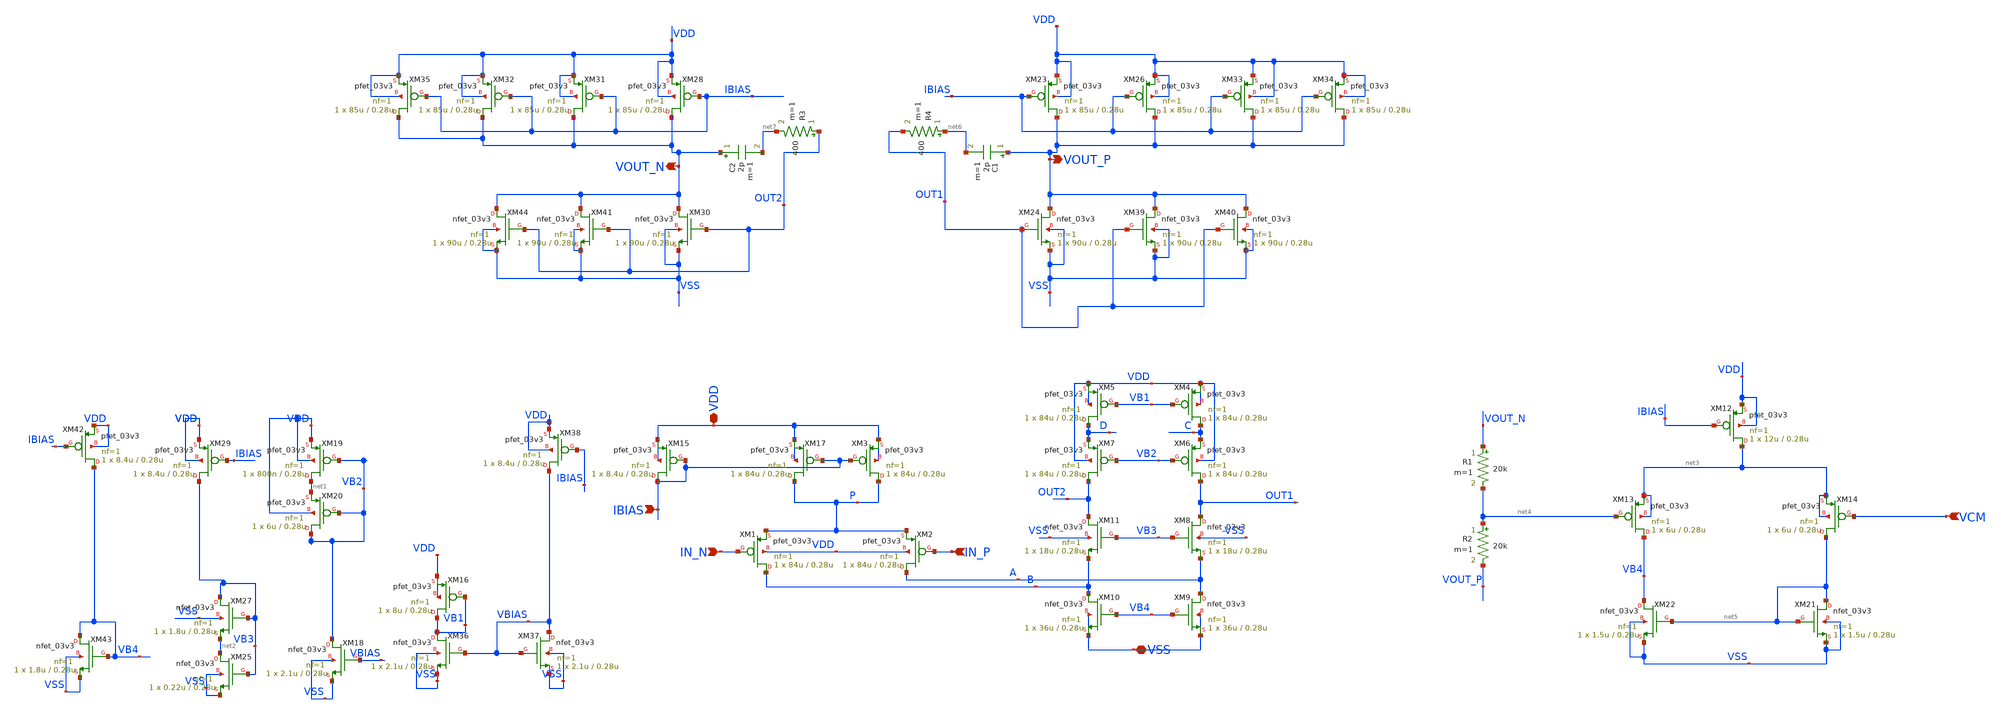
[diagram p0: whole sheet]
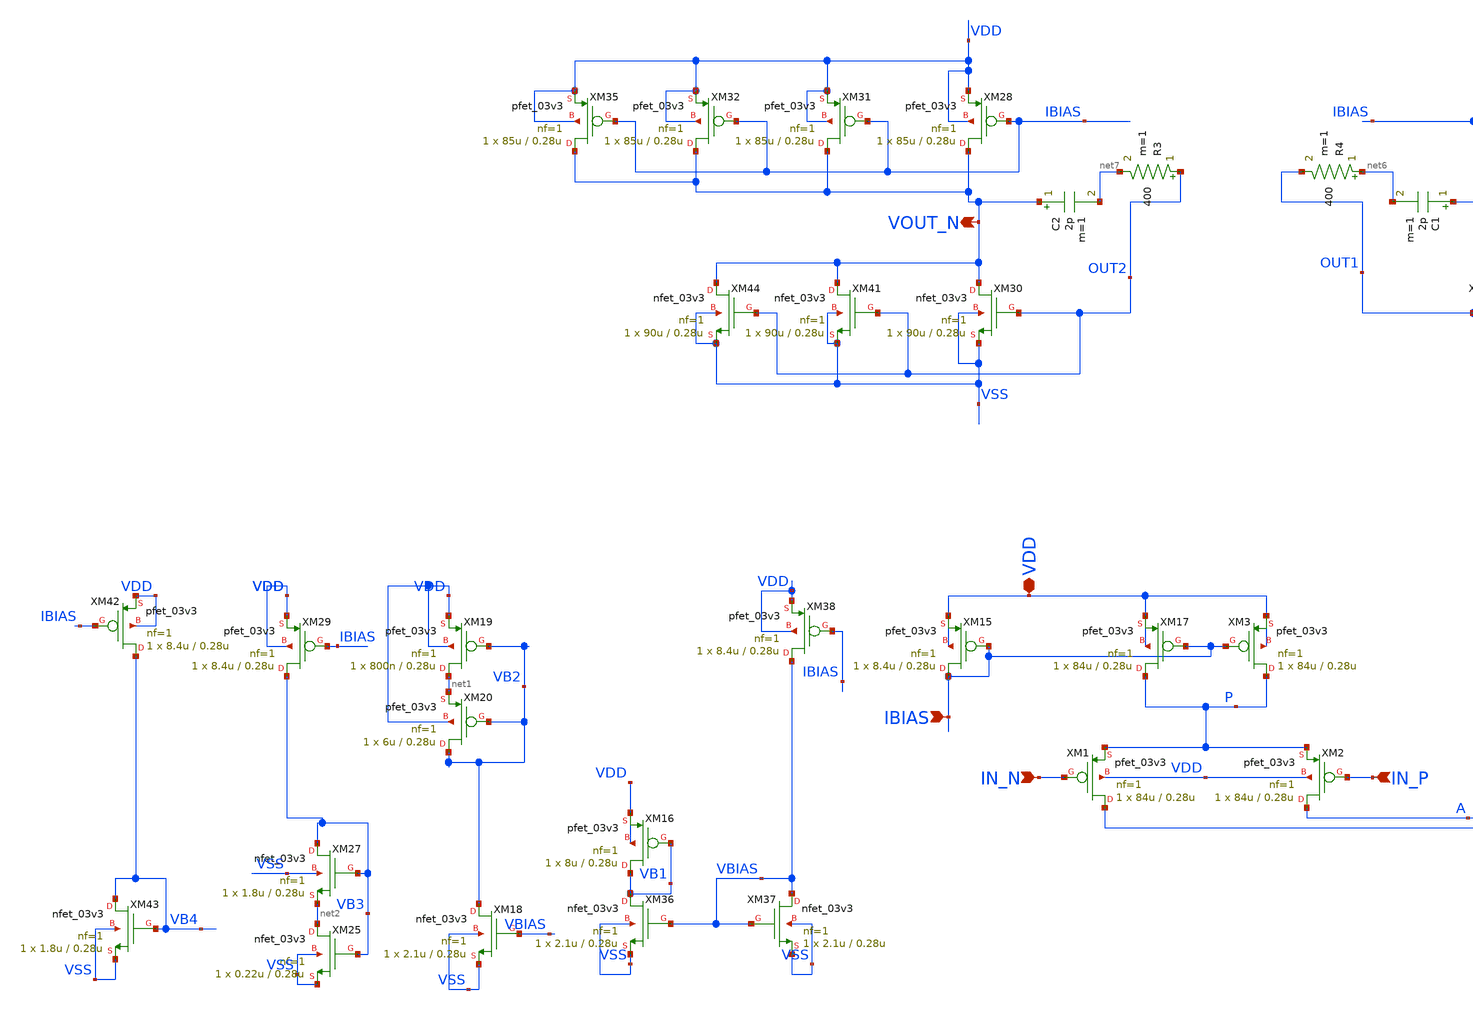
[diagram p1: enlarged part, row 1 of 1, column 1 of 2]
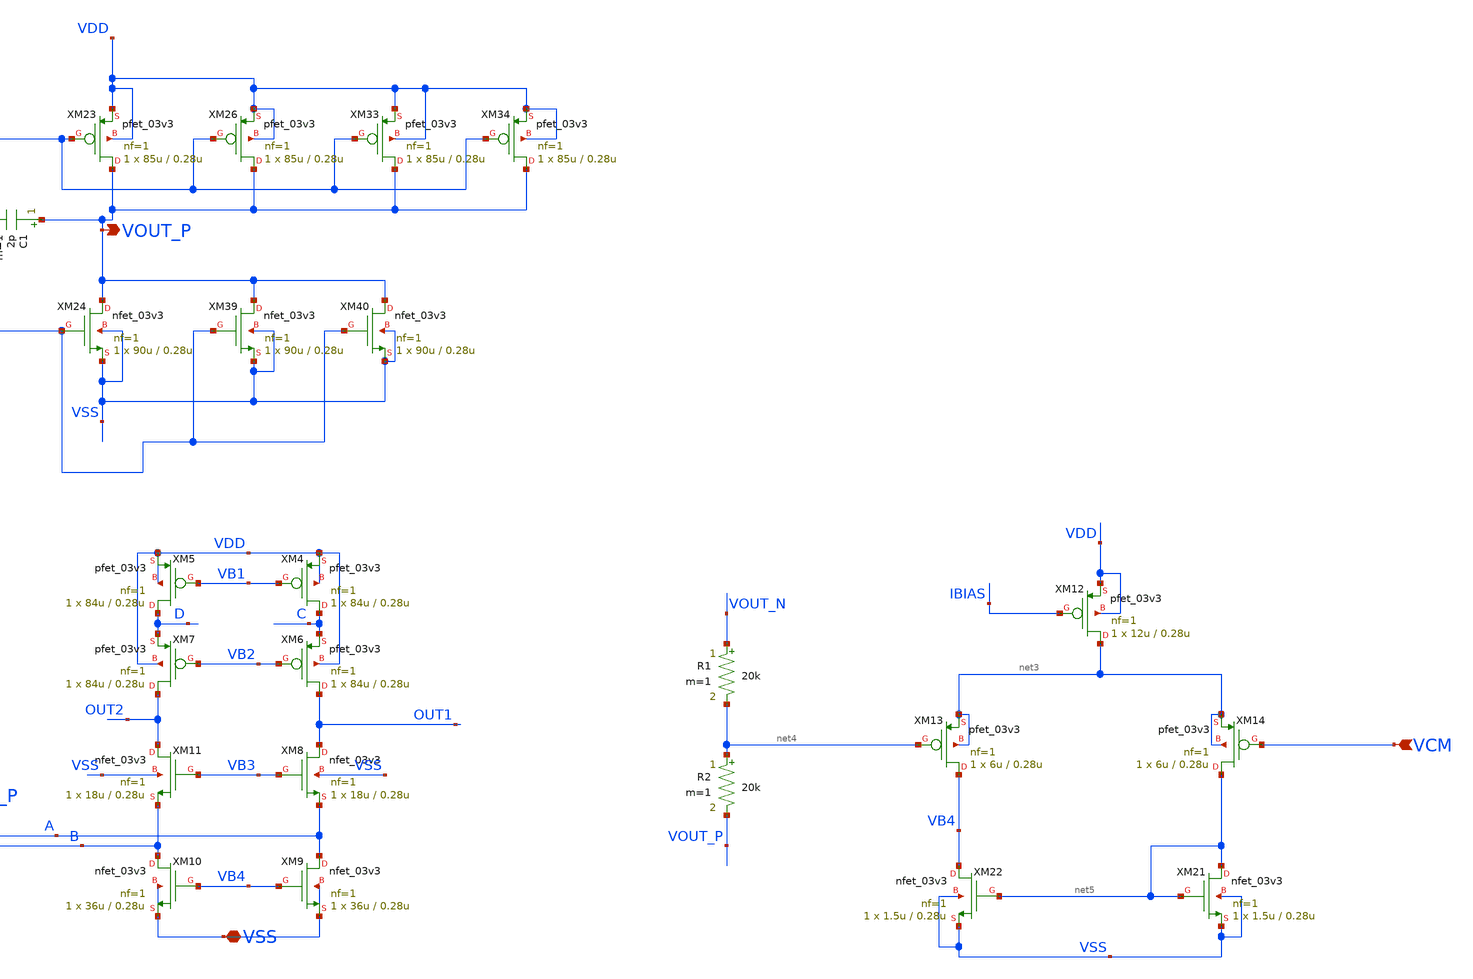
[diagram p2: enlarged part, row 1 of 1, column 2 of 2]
** sch_path: AWG_OUTPUT_AND_MUX_PAKISTAN_05/xschem/OPAMP_PMOS_FINAL1.sch
**.subckt OPAMP_PMOS_FINAL1 VDD VOUT_P VOUT_N VSS IN_N IN_P IBIAS VCM
*.iopin VDD
*.opin VOUT_P
*.opin VOUT_N
*.iopin VSS
*.ipin IN_N
*.ipin IN_P
*.ipin IBIAS
*.ipin VCM
XM1 B IN_N P VDD pfet_03v3 L=0.28u W=84u nf=1 ad='int((nf+1)/2) * W/nf * 0.18u' as='int((nf+2)/2) * W/nf * 0.18u'
+ pd='2*int((nf+1)/2) * (W/nf + 0.18u)' ps='2*int((nf+2)/2) * (W/nf + 0.18u)' nrd='0.18u / W' nrs='0.18u / W'
+ sa=0 sb=0 sd=0 m=1
XM2 A IN_P P VDD pfet_03v3 L=0.28u W=84u nf=1 ad='int((nf+1)/2) * W/nf * 0.18u' as='int((nf+2)/2) * W/nf * 0.18u'
+ pd='2*int((nf+1)/2) * (W/nf + 0.18u)' ps='2*int((nf+2)/2) * (W/nf + 0.18u)' nrd='0.18u / W' nrs='0.18u / W'
+ sa=0 sb=0 sd=0 m=1
XM3 P IBIAS VDD VDD pfet_03v3 L=0.28u W=84u nf=1 ad='int((nf+1)/2) * W/nf * 0.18u' as='int((nf+2)/2) * W/nf * 0.18u'
+ pd='2*int((nf+1)/2) * (W/nf + 0.18u)' ps='2*int((nf+2)/2) * (W/nf + 0.18u)' nrd='0.18u / W' nrs='0.18u / W'
+ sa=0 sb=0 sd=0 m=1
XM4 C VB1 VDD VDD pfet_03v3 L=0.28u W=84u nf=1 ad='int((nf+1)/2) * W/nf * 0.18u' as='int((nf+2)/2) * W/nf * 0.18u'
+ pd='2*int((nf+1)/2) * (W/nf + 0.18u)' ps='2*int((nf+2)/2) * (W/nf + 0.18u)' nrd='0.18u / W' nrs='0.18u / W'
+ sa=0 sb=0 sd=0 m=1
XM5 D VB1 VDD VDD pfet_03v3 L=0.28u W=84u nf=1 ad='int((nf+1)/2) * W/nf * 0.18u' as='int((nf+2)/2) * W/nf * 0.18u'
+ pd='2*int((nf+1)/2) * (W/nf + 0.18u)' ps='2*int((nf+2)/2) * (W/nf + 0.18u)' nrd='0.18u / W' nrs='0.18u / W'
+ sa=0 sb=0 sd=0 m=1
XM6 OUT1 VB2 C VDD pfet_03v3 L=0.28u W=84u nf=1 ad='int((nf+1)/2) * W/nf * 0.18u' as='int((nf+2)/2) * W/nf * 0.18u'
+ pd='2*int((nf+1)/2) * (W/nf + 0.18u)' ps='2*int((nf+2)/2) * (W/nf + 0.18u)' nrd='0.18u / W' nrs='0.18u / W'
+ sa=0 sb=0 sd=0 m=1
XM7 OUT2 VB2 D VDD pfet_03v3 L=0.28u W=84u nf=1 ad='int((nf+1)/2) * W/nf * 0.18u' as='int((nf+2)/2) * W/nf * 0.18u'
+ pd='2*int((nf+1)/2) * (W/nf + 0.18u)' ps='2*int((nf+2)/2) * (W/nf + 0.18u)' nrd='0.18u / W' nrs='0.18u / W'
+ sa=0 sb=0 sd=0 m=1
XM8 OUT1 VB3 A VSS nfet_03v3 L=0.28u W=18u nf=1 ad='int((nf+1)/2) * W/nf * 0.18u' as='int((nf+2)/2) * W/nf * 0.18u'
+ pd='2*int((nf+1)/2) * (W/nf + 0.18u)' ps='2*int((nf+2)/2) * (W/nf + 0.18u)' nrd='0.18u / W' nrs='0.18u / W'
+ sa=0 sb=0 sd=0 m=1
XM9 A VB4 VSS VSS nfet_03v3 L=0.28u W=36u nf=1 ad='int((nf+1)/2) * W/nf * 0.18u' as='int((nf+2)/2) * W/nf * 0.18u'
+ pd='2*int((nf+1)/2) * (W/nf + 0.18u)' ps='2*int((nf+2)/2) * (W/nf + 0.18u)' nrd='0.18u / W' nrs='0.18u / W'
+ sa=0 sb=0 sd=0 m=1
XM10 B VB4 VSS VSS nfet_03v3 L=0.28u W=36u nf=1 ad='int((nf+1)/2) * W/nf * 0.18u' as='int((nf+2)/2) * W/nf * 0.18u'
+ pd='2*int((nf+1)/2) * (W/nf + 0.18u)' ps='2*int((nf+2)/2) * (W/nf + 0.18u)' nrd='0.18u / W' nrs='0.18u / W'
+ sa=0 sb=0 sd=0 m=1
XM17 P IBIAS VDD VDD pfet_03v3 L=0.28u W=84u nf=1 ad='int((nf+1)/2) * W/nf * 0.18u' as='int((nf+2)/2) * W/nf * 0.18u'
+ pd='2*int((nf+1)/2) * (W/nf + 0.18u)' ps='2*int((nf+2)/2) * (W/nf + 0.18u)' nrd='0.18u / W' nrs='0.18u / W'
+ sa=0 sb=0 sd=0 m=1
XM11 OUT2 VB3 B VSS nfet_03v3 L=0.28u W=18u nf=1 ad='int((nf+1)/2) * W/nf * 0.18u' as='int((nf+2)/2) * W/nf * 0.18u'
+ pd='2*int((nf+1)/2) * (W/nf + 0.18u)' ps='2*int((nf+2)/2) * (W/nf + 0.18u)' nrd='0.18u / W' nrs='0.18u / W'
+ sa=0 sb=0 sd=0 m=1
XM36 VB1 VBIAS VSS VSS nfet_03v3 L=0.28u W=2.1u nf=1 ad='int((nf+1)/2) * W/nf * 0.18u' as='int((nf+2)/2) * W/nf * 0.18u'
+ pd='2*int((nf+1)/2) * (W/nf + 0.18u)' ps='2*int((nf+2)/2) * (W/nf + 0.18u)' nrd='0.18u / W' nrs='0.18u / W'
+ sa=0 sb=0 sd=0 m=1
XM37 VBIAS VBIAS VSS VSS nfet_03v3 L=0.28u W=2.1u nf=1 ad='int((nf+1)/2) * W/nf * 0.18u' as='int((nf+2)/2) * W/nf * 0.18u'
+ pd='2*int((nf+1)/2) * (W/nf + 0.18u)' ps='2*int((nf+2)/2) * (W/nf + 0.18u)' nrd='0.18u / W' nrs='0.18u / W'
+ sa=0 sb=0 sd=0 m=1
XM38 VBIAS IBIAS VDD VDD pfet_03v3 L=0.28u W=8.4u nf=1 ad='int((nf+1)/2) * W/nf * 0.18u' as='int((nf+2)/2) * W/nf * 0.18u'
+ pd='2*int((nf+1)/2) * (W/nf + 0.18u)' ps='2*int((nf+2)/2) * (W/nf + 0.18u)' nrd='0.18u / W' nrs='0.18u / W'
+ sa=0 sb=0 sd=0 m=1
XM42 VB4 IBIAS VDD VDD pfet_03v3 L=0.28u W=8.4u nf=1 ad='int((nf+1)/2) * W/nf * 0.18u' as='int((nf+2)/2) * W/nf * 0.18u'
+ pd='2*int((nf+1)/2) * (W/nf + 0.18u)' ps='2*int((nf+2)/2) * (W/nf + 0.18u)' nrd='0.18u / W' nrs='0.18u / W'
+ sa=0 sb=0 sd=0 m=1
XM43 VB4 VB4 VSS VSS nfet_03v3 L=0.28u W=1.8u nf=1 ad='int((nf+1)/2) * W/nf * 0.18u' as='int((nf+2)/2) * W/nf * 0.18u'
+ pd='2*int((nf+1)/2) * (W/nf + 0.18u)' ps='2*int((nf+2)/2) * (W/nf + 0.18u)' nrd='0.18u / W' nrs='0.18u / W'
+ sa=0 sb=0 sd=0 m=1
XM15 IBIAS IBIAS VDD VDD pfet_03v3 L=0.28u W=8.4u nf=1 ad='int((nf+1)/2) * W/nf * 0.18u' as='int((nf+2)/2) * W/nf * 0.18u'
+ pd='2*int((nf+1)/2) * (W/nf + 0.18u)' ps='2*int((nf+2)/2) * (W/nf + 0.18u)' nrd='0.18u / W' nrs='0.18u / W'
+ sa=0 sb=0 sd=0 m=1
XM16 VB1 VB1 VDD VDD pfet_03v3 L=0.28u W=8u nf=1 ad='int((nf+1)/2) * W/nf * 0.18u' as='int((nf+2)/2) * W/nf * 0.18u'
+ pd='2*int((nf+1)/2) * (W/nf + 0.18u)' ps='2*int((nf+2)/2) * (W/nf + 0.18u)' nrd='0.18u / W' nrs='0.18u / W'
+ sa=0 sb=0 sd=0 m=1
XM18 VB2 VBIAS VSS VSS nfet_03v3 L=0.28u W=2.1u nf=1 ad='int((nf+1)/2) * W/nf * 0.18u' as='int((nf+2)/2) * W/nf * 0.18u'
+ pd='2*int((nf+1)/2) * (W/nf + 0.18u)' ps='2*int((nf+2)/2) * (W/nf + 0.18u)' nrd='0.18u / W' nrs='0.18u / W'
+ sa=0 sb=0 sd=0 m=1
XM19 net1 VB2 VDD VDD pfet_03v3 L=0.28u W=800n nf=1 ad='int((nf+1)/2) * W/nf * 0.18u' as='int((nf+2)/2) * W/nf * 0.18u'
+ pd='2*int((nf+1)/2) * (W/nf + 0.18u)' ps='2*int((nf+2)/2) * (W/nf + 0.18u)' nrd='0.18u / W' nrs='0.18u / W'
+ sa=0 sb=0 sd=0 m=1
XM20 VB2 VB2 net1 VDD pfet_03v3 L=0.28u W=6u nf=1 ad='int((nf+1)/2) * W/nf * 0.18u' as='int((nf+2)/2) * W/nf * 0.18u'
+ pd='2*int((nf+1)/2) * (W/nf + 0.18u)' ps='2*int((nf+2)/2) * (W/nf + 0.18u)' nrd='0.18u / W' nrs='0.18u / W'
+ sa=0 sb=0 sd=0 m=1
XM25 net2 VB3 VSS VSS nfet_03v3 L=0.28u W=0.22u nf=1 ad='int((nf+1)/2) * W/nf * 0.18u' as='int((nf+2)/2) * W/nf * 0.18u'
+ pd='2*int((nf+1)/2) * (W/nf + 0.18u)' ps='2*int((nf+2)/2) * (W/nf + 0.18u)' nrd='0.18u / W' nrs='0.18u / W'
+ sa=0 sb=0 sd=0 m=1
XM27 VB3 VB3 net2 VSS nfet_03v3 L=0.28u W=1.8u nf=1 ad='int((nf+1)/2) * W/nf * 0.18u' as='int((nf+2)/2) * W/nf * 0.18u'
+ pd='2*int((nf+1)/2) * (W/nf + 0.18u)' ps='2*int((nf+2)/2) * (W/nf + 0.18u)' nrd='0.18u / W' nrs='0.18u / W'
+ sa=0 sb=0 sd=0 m=1
XM29 VB3 IBIAS VDD VDD pfet_03v3 L=0.28u W=8.4u nf=1 ad='int((nf+1)/2) * W/nf * 0.18u' as='int((nf+2)/2) * W/nf * 0.18u'
+ pd='2*int((nf+1)/2) * (W/nf + 0.18u)' ps='2*int((nf+2)/2) * (W/nf + 0.18u)' nrd='0.18u / W' nrs='0.18u / W'
+ sa=0 sb=0 sd=0 m=1
XM12 net3 IBIAS VDD VDD pfet_03v3 L=0.28u W=12u nf=1 ad='int((nf+1)/2) * W/nf * 0.18u' as='int((nf+2)/2) * W/nf * 0.18u'
+ pd='2*int((nf+1)/2) * (W/nf + 0.18u)' ps='2*int((nf+2)/2) * (W/nf + 0.18u)' nrd='0.18u / W' nrs='0.18u / W'
+ sa=0 sb=0 sd=0 m=1
XM13 VB4 net4 net3 net3 pfet_03v3 L=0.28u W=6u nf=1 ad='int((nf+1)/2) * W/nf * 0.18u' as='int((nf+2)/2) * W/nf * 0.18u'
+ pd='2*int((nf+1)/2) * (W/nf + 0.18u)' ps='2*int((nf+2)/2) * (W/nf + 0.18u)' nrd='0.18u / W' nrs='0.18u / W'
+ sa=0 sb=0 sd=0 m=1
XM14 net5 VCM net3 net3 pfet_03v3 L=0.28u W=6u nf=1 ad='int((nf+1)/2) * W/nf * 0.18u' as='int((nf+2)/2) * W/nf * 0.18u'
+ pd='2*int((nf+1)/2) * (W/nf + 0.18u)' ps='2*int((nf+2)/2) * (W/nf + 0.18u)' nrd='0.18u / W' nrs='0.18u / W'
+ sa=0 sb=0 sd=0 m=1
XM21 net5 net5 VSS VSS nfet_03v3 L=0.28u W=1.5u nf=1 ad='int((nf+1)/2) * W/nf * 0.18u' as='int((nf+2)/2) * W/nf * 0.18u'
+ pd='2*int((nf+1)/2) * (W/nf + 0.18u)' ps='2*int((nf+2)/2) * (W/nf + 0.18u)' nrd='0.18u / W' nrs='0.18u / W'
+ sa=0 sb=0 sd=0 m=1
XM22 VB4 net5 VSS VSS nfet_03v3 L=0.28u W=1.5u nf=1 ad='int((nf+1)/2) * W/nf * 0.18u' as='int((nf+2)/2) * W/nf * 0.18u'
+ pd='2*int((nf+1)/2) * (W/nf + 0.18u)' ps='2*int((nf+2)/2) * (W/nf + 0.18u)' nrd='0.18u / W' nrs='0.18u / W'
+ sa=0 sb=0 sd=0 m=1
R1 VOUT_N net4 20k m=1
R2 net4 VOUT_P 20k m=1
XM23 VOUT_P IBIAS VDD VDD pfet_03v3 L=0.28u W=85u nf=1 ad='int((nf+1)/2) * W/nf * 0.18u' as='int((nf+2)/2) * W/nf * 0.18u'
+ pd='2*int((nf+1)/2) * (W/nf + 0.18u)' ps='2*int((nf+2)/2) * (W/nf + 0.18u)' nrd='0.18u / W' nrs='0.18u / W'
+ sa=0 sb=0 sd=0 m=1
XM24 VOUT_P OUT1 VSS VSS nfet_03v3 L=0.28u W=90u nf=1 ad='int((nf+1)/2) * W/nf * 0.18u' as='int((nf+2)/2) * W/nf * 0.18u'
+ pd='2*int((nf+1)/2) * (W/nf + 0.18u)' ps='2*int((nf+2)/2) * (W/nf + 0.18u)' nrd='0.18u / W' nrs='0.18u / W'
+ sa=0 sb=0 sd=0 m=1
C1 VOUT_P net6 2p m=1
XM26 VOUT_P IBIAS VDD VDD pfet_03v3 L=0.28u W=85u nf=1 ad='int((nf+1)/2) * W/nf * 0.18u' as='int((nf+2)/2) * W/nf * 0.18u'
+ pd='2*int((nf+1)/2) * (W/nf + 0.18u)' ps='2*int((nf+2)/2) * (W/nf + 0.18u)' nrd='0.18u / W' nrs='0.18u / W'
+ sa=0 sb=0 sd=0 m=1
XM28 VOUT_N IBIAS VDD VDD pfet_03v3 L=0.28u W=85u nf=1 ad='int((nf+1)/2) * W/nf * 0.18u' as='int((nf+2)/2) * W/nf * 0.18u'
+ pd='2*int((nf+1)/2) * (W/nf + 0.18u)' ps='2*int((nf+2)/2) * (W/nf + 0.18u)' nrd='0.18u / W' nrs='0.18u / W'
+ sa=0 sb=0 sd=0 m=1
XM30 VOUT_N OUT2 VSS VSS nfet_03v3 L=0.28u W=90u nf=1 ad='int((nf+1)/2) * W/nf * 0.18u' as='int((nf+2)/2) * W/nf * 0.18u'
+ pd='2*int((nf+1)/2) * (W/nf + 0.18u)' ps='2*int((nf+2)/2) * (W/nf + 0.18u)' nrd='0.18u / W' nrs='0.18u / W'
+ sa=0 sb=0 sd=0 m=1
C2 VOUT_N net7 2p m=1
XM31 VOUT_N IBIAS VDD VDD pfet_03v3 L=0.28u W=85u nf=1 ad='int((nf+1)/2) * W/nf * 0.18u' as='int((nf+2)/2) * W/nf * 0.18u'
+ pd='2*int((nf+1)/2) * (W/nf + 0.18u)' ps='2*int((nf+2)/2) * (W/nf + 0.18u)' nrd='0.18u / W' nrs='0.18u / W'
+ sa=0 sb=0 sd=0 m=1
R3 OUT2 net7 400 m=1
R4 net6 OUT1 400 m=1
XM32 VOUT_N IBIAS VDD VDD pfet_03v3 L=0.28u W=85u nf=1 ad='int((nf+1)/2) * W/nf * 0.18u' as='int((nf+2)/2) * W/nf * 0.18u'
+ pd='2*int((nf+1)/2) * (W/nf + 0.18u)' ps='2*int((nf+2)/2) * (W/nf + 0.18u)' nrd='0.18u / W' nrs='0.18u / W'
+ sa=0 sb=0 sd=0 m=1
XM33 VOUT_P IBIAS VDD VDD pfet_03v3 L=0.28u W=85u nf=1 ad='int((nf+1)/2) * W/nf * 0.18u' as='int((nf+2)/2) * W/nf * 0.18u'
+ pd='2*int((nf+1)/2) * (W/nf + 0.18u)' ps='2*int((nf+2)/2) * (W/nf + 0.18u)' nrd='0.18u / W' nrs='0.18u / W'
+ sa=0 sb=0 sd=0 m=1
XM34 VOUT_P IBIAS VDD VDD pfet_03v3 L=0.28u W=85u nf=1 ad='int((nf+1)/2) * W/nf * 0.18u' as='int((nf+2)/2) * W/nf * 0.18u'
+ pd='2*int((nf+1)/2) * (W/nf + 0.18u)' ps='2*int((nf+2)/2) * (W/nf + 0.18u)' nrd='0.18u / W' nrs='0.18u / W'
+ sa=0 sb=0 sd=0 m=1
XM35 VOUT_N IBIAS VDD VDD pfet_03v3 L=0.28u W=85u nf=1 ad='int((nf+1)/2) * W/nf * 0.18u' as='int((nf+2)/2) * W/nf * 0.18u'
+ pd='2*int((nf+1)/2) * (W/nf + 0.18u)' ps='2*int((nf+2)/2) * (W/nf + 0.18u)' nrd='0.18u / W' nrs='0.18u / W'
+ sa=0 sb=0 sd=0 m=1
XM39 VOUT_P OUT1 VSS VSS nfet_03v3 L=0.28u W=90u nf=1 ad='int((nf+1)/2) * W/nf * 0.18u' as='int((nf+2)/2) * W/nf * 0.18u'
+ pd='2*int((nf+1)/2) * (W/nf + 0.18u)' ps='2*int((nf+2)/2) * (W/nf + 0.18u)' nrd='0.18u / W' nrs='0.18u / W'
+ sa=0 sb=0 sd=0 m=1
XM40 VOUT_P OUT1 VSS VSS nfet_03v3 L=0.28u W=90u nf=1 ad='int((nf+1)/2) * W/nf * 0.18u' as='int((nf+2)/2) * W/nf * 0.18u'
+ pd='2*int((nf+1)/2) * (W/nf + 0.18u)' ps='2*int((nf+2)/2) * (W/nf + 0.18u)' nrd='0.18u / W' nrs='0.18u / W'
+ sa=0 sb=0 sd=0 m=1
XM41 VOUT_N OUT2 VSS VSS nfet_03v3 L=0.28u W=90u nf=1 ad='int((nf+1)/2) * W/nf * 0.18u' as='int((nf+2)/2) * W/nf * 0.18u'
+ pd='2*int((nf+1)/2) * (W/nf + 0.18u)' ps='2*int((nf+2)/2) * (W/nf + 0.18u)' nrd='0.18u / W' nrs='0.18u / W'
+ sa=0 sb=0 sd=0 m=1
XM44 VOUT_N OUT2 VSS VSS nfet_03v3 L=0.28u W=90u nf=1 ad='int((nf+1)/2) * W/nf * 0.18u' as='int((nf+2)/2) * W/nf * 0.18u'
+ pd='2*int((nf+1)/2) * (W/nf + 0.18u)' ps='2*int((nf+2)/2) * (W/nf + 0.18u)' nrd='0.18u / W' nrs='0.18u / W'
+ sa=0 sb=0 sd=0 m=1
**.ends
.end
